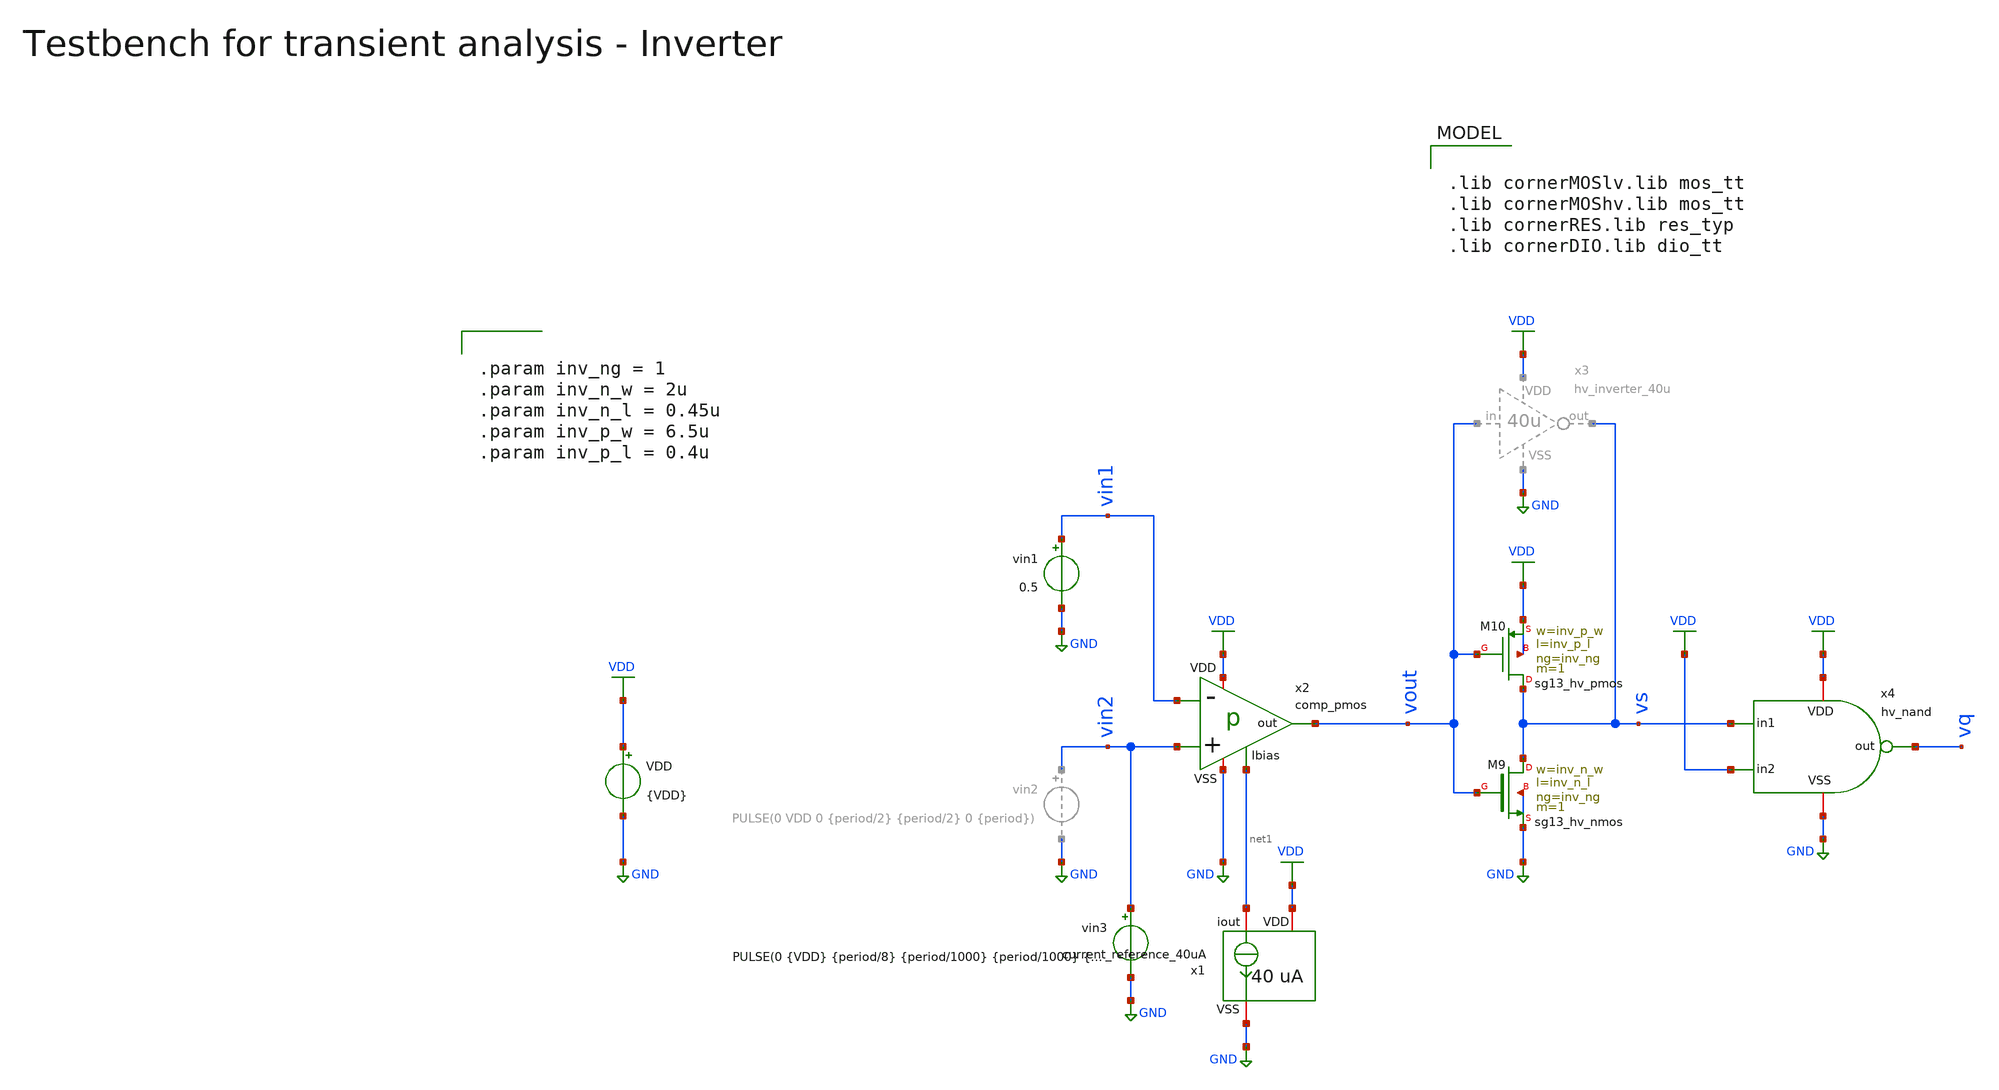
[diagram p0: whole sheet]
** sch_path: macros/heichips26_vcr/macros/switched_capacitor/testbenches/xschem/tb_comp_pmos_tran.sch
**.subckt tb_comp_pmos_tran
VDD VDD GND {VDD}
vin1 vin1 GND 0.5
x2 vout vin1 vin2 VDD net1 GND comp_pmos
x1 VDD net1 GND current_reference_40uA
vin3 vin2 GND PULSE(0 {VDD} {period/8} {period/1000} {period/1000} {period/2} {period})
XM9 vs vout GND GND sg13_hv_nmos w=inv_n_w l=inv_n_l ng=inv_ng m=1 mm_ok=1
XM10 vs vout VDD VDD sg13_hv_pmos w=inv_p_w l=inv_p_l ng=inv_ng m=1 mm_ok=1
x4 VDD vs vq VDD GND hv_nand
**** begin user architecture code


.param VDD=3.3
.csparam VDD=VDD
.param Vcm=VDD/2
.param temp=27
.param Cload=10p
.param Rload=1k

.param period = 5n
.param ton    = {period*2}
.csparam tstop  = {1.2*period}
.csparam tstep  = {period/100}

.options savecurrents klu method=gear reltol=1e-4 abstol=1e-15 gmin=1e-15
.control

save all

* Operating Point Analysis
op
remzerovec
write @schname\.raw
set appendwrite

* Transient Analysis
tran {$&tstep} {$&tstop}
write @schname\.raw

* Plotting
plot vin1+4 vin2+4 vout vs vq+4

* Write Data
unset appendwrite
set wr_vecnames
set wr_singlescale
*wrdata ../plot_simulations/data/@schname\.txt v(vin1) v(vin2) v(vout)

*quit
.endc



.lib cornerMOSlv.lib mos_tt
.lib cornerMOShv.lib mos_tt
.lib cornerRES.lib res_typ
.lib cornerDIO.lib dio_tt



.param inv_ng = 1
.param inv_n_w = 2u
.param inv_n_l = 0.45u
.param inv_p_w = 6.5u
.param inv_p_l = 0.4u


**** end user architecture code
**.ends

* expanding   symbol:  comp_pmos.sym # of pins=6
** sym_path: macros/heichips26_vcr/macros/switched_capacitor/schematic/xschem/comp_pmos.sym
** sch_path: macros/heichips26_vcr/macros/switched_capacitor/schematic/xschem/comp_pmos.sch
.subckt comp_pmos out - + VDD Ibias VSS
*.iopin VDD
*.iopin VSS
*.ipin Ibias
*.opin out
*.ipin +
*.ipin -
**** begin user architecture code


.param n_w = 1.2u
.param n_l = 1.5u
.param p_w = 2u
.param p_l = 0.4u
.param bcm = 1


**** end user architecture code
XM9 net1 Ibias VDD VDD sg13_hv_pmos w=bcm*p_w l=p_l ng=1 m=1 mm_ok=1
XM10 out Ibias VDD VDD sg13_hv_pmos w=bcm*p_w l=p_l ng=1 m=1 mm_ok=1
XM11 Ibias Ibias VDD VDD sg13_hv_pmos w=p_w l=p_l ng=1 m=1 mm_ok=1
XM12 net3 + net1 VDD sg13_hv_pmos w=p_w l=p_l ng=1 m=1 mm_ok=1
XM13 net2 - net1 VDD sg13_hv_pmos w=p_w l=p_l ng=1 m=1 mm_ok=1
XM14 net3 net2 VSS VSS sg13_hv_nmos w=n_w l=n_l ng=1 m=1 mm_ok=1
XM15 net2 net2 VSS VSS sg13_hv_nmos w=n_w l=n_l ng=1 m=1 mm_ok=1
XM16 out net3 VSS VSS sg13_hv_nmos w=n_w l=n_l ng=1 m=1 mm_ok=1
.ends


* expanding   symbol:  current_reference_40uA.sym # of pins=3
** sym_path: macros/heichips26_vcr/macros/switched_capacitor/schematic/xschem/current_reference_40uA.sym
** sch_path: macros/heichips26_vcr/macros/switched_capacitor/schematic/xschem/current_reference_40uA.sch
.subckt current_reference_40uA VDD iout VSS
*.iopin VSS
*.iopin VDD
*.iopin iout
XM8 net2 net2 VSS VSS sg13_hv_nmos w=n_w l=n_l ng=1 m=1 mm_ok=1
XM6 net2 net1 VDD VDD sg13_hv_pmos w=p_w l=p_l ng=1 m=1 mm_ok=1
XM1 net1 net1 VDD VDD sg13_hv_pmos w=p_w l=p_l ng=1 m=1 mm_ok=1
XM3 net1 net2 net3 VSS sg13_hv_nmos w=n_w l=n_l ng=1 m=1 mm_ok=1
XR2 net4 VSS VSS rppd w=2e-6 l=21.9e-6 m=1 b=0 mm_ok=1
XM2 net1 net2 net3 VSS sg13_hv_nmos w=n_w l=n_l ng=1 m=1 mm_ok=1
XM4 net1 net2 net3 VSS sg13_hv_nmos w=n_w l=n_l ng=1 m=1 mm_ok=1
XM5 net1 net2 net3 VSS sg13_hv_nmos w=n_w l=n_l ng=1 m=1 mm_ok=1
XM7 iout net2 VSS VSS sg13_hv_nmos w=n_w l=n_l ng=1 m=1 mm_ok=1
XR3 net3 net4 VSS rsil w=0.5e-6 l=365e-6 m=1 mm_ok=1
**** begin user architecture code


.param n_w = 6u
.param n_l = 5u
.param p_w = 10u
.param p_l = 2u


**** end user architecture code
.ends


* expanding   symbol:  hv_inverter_40u.sym # of pins=4
** sym_path: macros/heichips26_vcr/macros/switched_capacitor/schematic/xschem/hv_inverter_40u.sym
** sch_path: macros/heichips26_vcr/macros/switched_capacitor/schematic/xschem/hv_inverter_40u.sch
.subckt hv_inverter_40u VDD in out VSS
*.ipin in
*.iopin VDD
*.iopin VSS
*.opin out
XM2 out in VSS VSS sg13_hv_nmos w={n_w} l={n_l} ng={ng} m=1 mm_ok=1
XM3 out in VDD VDD sg13_hv_pmos w={p_w} l={p_l} ng={ng} m=1 mm_ok=1
**** begin user architecture code


.param w   = 10u
.param ng  = 4
.param n_ng = ng
.param n_w = {3u*n_ng}
.param n_l = 0.45u
.param p_ng = ng
.param p_w = {10u*p_ng}
.param p_l = 0.4u


**** end user architecture code
.ends


* expanding   symbol:  hv_nand.sym # of pins=5
** sym_path: macros/heichips26_vcr/macros/switched_capacitor/schematic/xschem/hv_nand.sym
** sch_path: macros/heichips26_vcr/macros/switched_capacitor/schematic/xschem/hv_nand.sch
.subckt hv_nand VDD in1 out in2 VSS
*.ipin in1
*.iopin VDD
*.iopin VSS
*.opin out
*.ipin in2
**** begin user architecture code


.param w   = 10u
.param ng  = 4
.param n_ng = ng
.param n_w = {3u*n_ng}
.param n_l = 0.45u
.param p_ng = ng
.param p_w = {10u*p_ng}
.param p_l = 0.4u


**** end user architecture code
XM2 out in1 net1 VSS sg13_hv_nmos w={n_w} l={n_l} ng={ng} m=1 mm_ok=1
XM3 out in2 VDD VDD sg13_hv_pmos w={p_w} l={p_l} ng={ng} m=1 mm_ok=1
XM1 net1 in2 VSS VSS sg13_hv_nmos w={n_w} l={n_l} ng={ng} m=1 mm_ok=1
XM4 out in1 VDD VDD sg13_hv_pmos w={p_w} l={p_l} ng={ng} m=1 mm_ok=1
.ends

.GLOBAL GND
.GLOBAL VDD
.end
